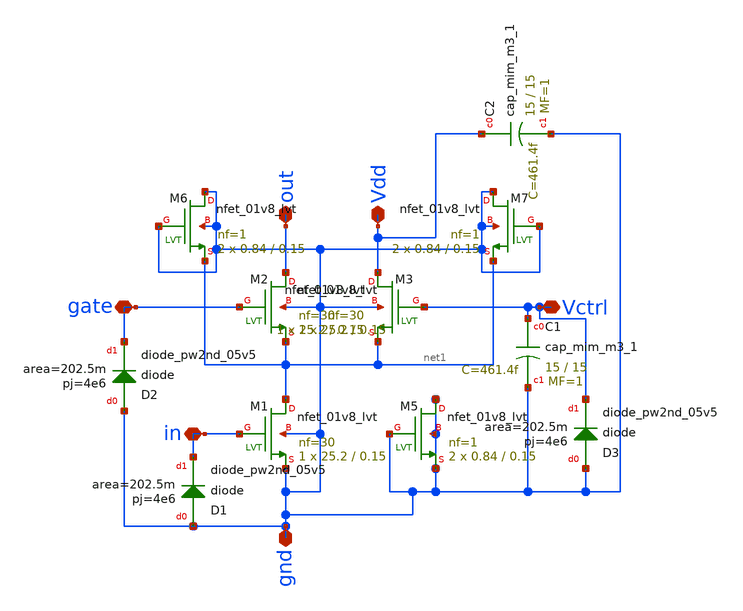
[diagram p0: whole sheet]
** sch_path: VGA_tapeout/xschem/VGA_core/VGA_gainCellv3.sch
**.subckt VGA_gainCellv3 in out gate Vdd Vctrl gnd
*.iopin in
*.iopin out
*.iopin gate
*.iopin Vdd
*.iopin Vctrl
*.iopin gnd
XM1 net1 in gnd gnd sky130_fd_pr__nfet_01v8_lvt L=0.15 W=25.2 nf=30 ad='int((nf+1)/2) * W/nf * 0.29'
+ as='int((nf+2)/2) * W/nf * 0.29' pd='2*int((nf+1)/2) * (W/nf + 0.29)' ps='2*int((nf+2)/2) * (W/nf + 0.29)'
+ nrd='0.29 / W' nrs='0.29 / W' sa=0 sb=0 sd=0 mult=1 m=1
XM2 out gate net1 gnd sky130_fd_pr__nfet_01v8_lvt L=0.15 W=25.2 nf=30 ad='int((nf+1)/2) * W/nf * 0.29'
+ as='int((nf+2)/2) * W/nf * 0.29' pd='2*int((nf+1)/2) * (W/nf + 0.29)' ps='2*int((nf+2)/2) * (W/nf + 0.29)'
+ nrd='0.29 / W' nrs='0.29 / W' sa=0 sb=0 sd=0 mult=1 m=1
XM3 Vdd Vctrl net1 gnd sky130_fd_pr__nfet_01v8_lvt L=0.15 W=25.2 nf=30 ad='int((nf+1)/2) * W/nf * 0.29'
+ as='int((nf+2)/2) * W/nf * 0.29' pd='2*int((nf+1)/2) * (W/nf + 0.29)' ps='2*int((nf+2)/2) * (W/nf + 0.29)'
+ nrd='0.29 / W' nrs='0.29 / W' sa=0 sb=0 sd=0 mult=1 m=1
XM5 gnd gnd gnd gnd sky130_fd_pr__nfet_01v8_lvt L=0.15 W=0.84 nf=1 ad='int((nf+1)/2) * W/nf * 0.29' as='int((nf+2)/2) * W/nf * 0.29'
+ pd='2*int((nf+1)/2) * (W/nf + 0.29)' ps='2*int((nf+2)/2) * (W/nf + 0.29)' nrd='0.29 / W' nrs='0.29 / W'
+ sa=0 sb=0 sd=0 mult=2 m=2
XM6 gnd gnd net1 gnd sky130_fd_pr__nfet_01v8_lvt L=0.15 W=0.84 nf=1 ad='int((nf+1)/2) * W/nf * 0.29'
+ as='int((nf+2)/2) * W/nf * 0.29' pd='2*int((nf+1)/2) * (W/nf + 0.29)' ps='2*int((nf+2)/2) * (W/nf + 0.29)'
+ nrd='0.29 / W' nrs='0.29 / W' sa=0 sb=0 sd=0 mult=2 m=2
XM7 gnd gnd net1 gnd sky130_fd_pr__nfet_01v8_lvt L=0.15 W=0.84 nf=1 ad='int((nf+1)/2) * W/nf * 0.29'
+ as='int((nf+2)/2) * W/nf * 0.29' pd='2*int((nf+1)/2) * (W/nf + 0.29)' ps='2*int((nf+2)/2) * (W/nf + 0.29)'
+ nrd='0.29 / W' nrs='0.29 / W' sa=0 sb=0 sd=0 mult=2 m=2
XC1 Vctrl gnd sky130_fd_pr__cap_mim_m3_1 W=15 L=15 MF=1 m=1
XC2 Vdd gnd sky130_fd_pr__cap_mim_m3_1 W=15 L=15 MF=1 m=1
XD1 gnd in sky130_fd_pr__diode_pw2nd_05v5 area=202.5m pj=4e6
XD2 gnd gate sky130_fd_pr__diode_pw2nd_05v5 area=202.5m pj=4e6
XD3 gnd Vctrl sky130_fd_pr__diode_pw2nd_05v5 area=202.5m pj=4e6
**.ends
.end
